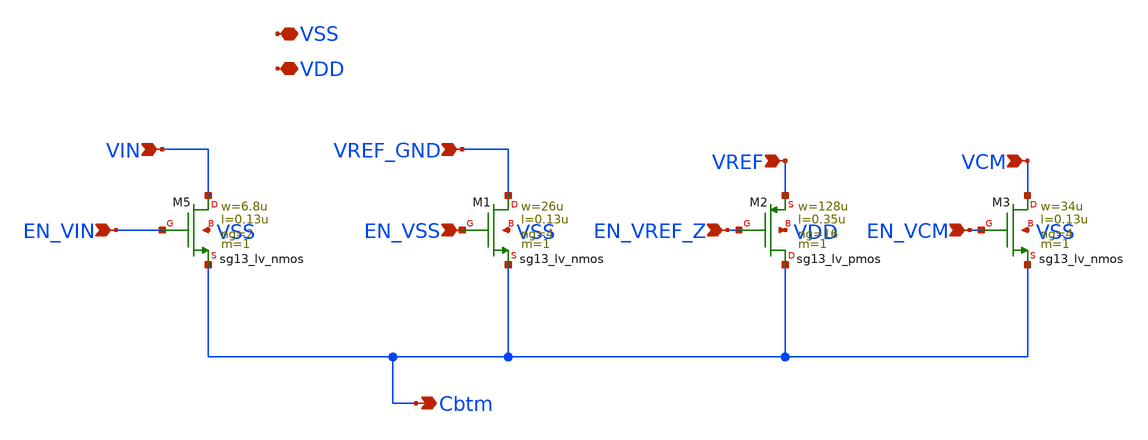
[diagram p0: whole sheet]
** sch_path: schematic/individual_switches/switch_C10.sch
**.subckt switch_C10 VIN EN_VIN VREF_GND EN_VSS Cbtm VSS VREF EN_VREF_Z EN_VCM VCM VDD
*.ipin VIN
*.ipin EN_VIN
*.ipin VREF_GND
*.ipin EN_VSS
*.opin Cbtm
*.iopin VSS
*.ipin VREF
*.ipin EN_VREF_Z
*.ipin EN_VCM
*.ipin VCM
*.iopin VDD
XM5 VIN EN_VIN Cbtm VSS sg13_lv_nmos w=6.8u l=0.13u ng=2 m=1 mm_ok=1
XM1 VREF_GND EN_VSS Cbtm VSS sg13_lv_nmos w=26u l=0.13u ng=4 m=1 mm_ok=1
XM2 Cbtm EN_VREF_Z VREF VDD sg13_lv_pmos w=128u l=0.35u ng=16 m=1 mm_ok=1
XM3 VCM EN_VCM Cbtm VSS sg13_lv_nmos w=34u l=0.13u ng=4 m=1 mm_ok=1
**.ends
.end
